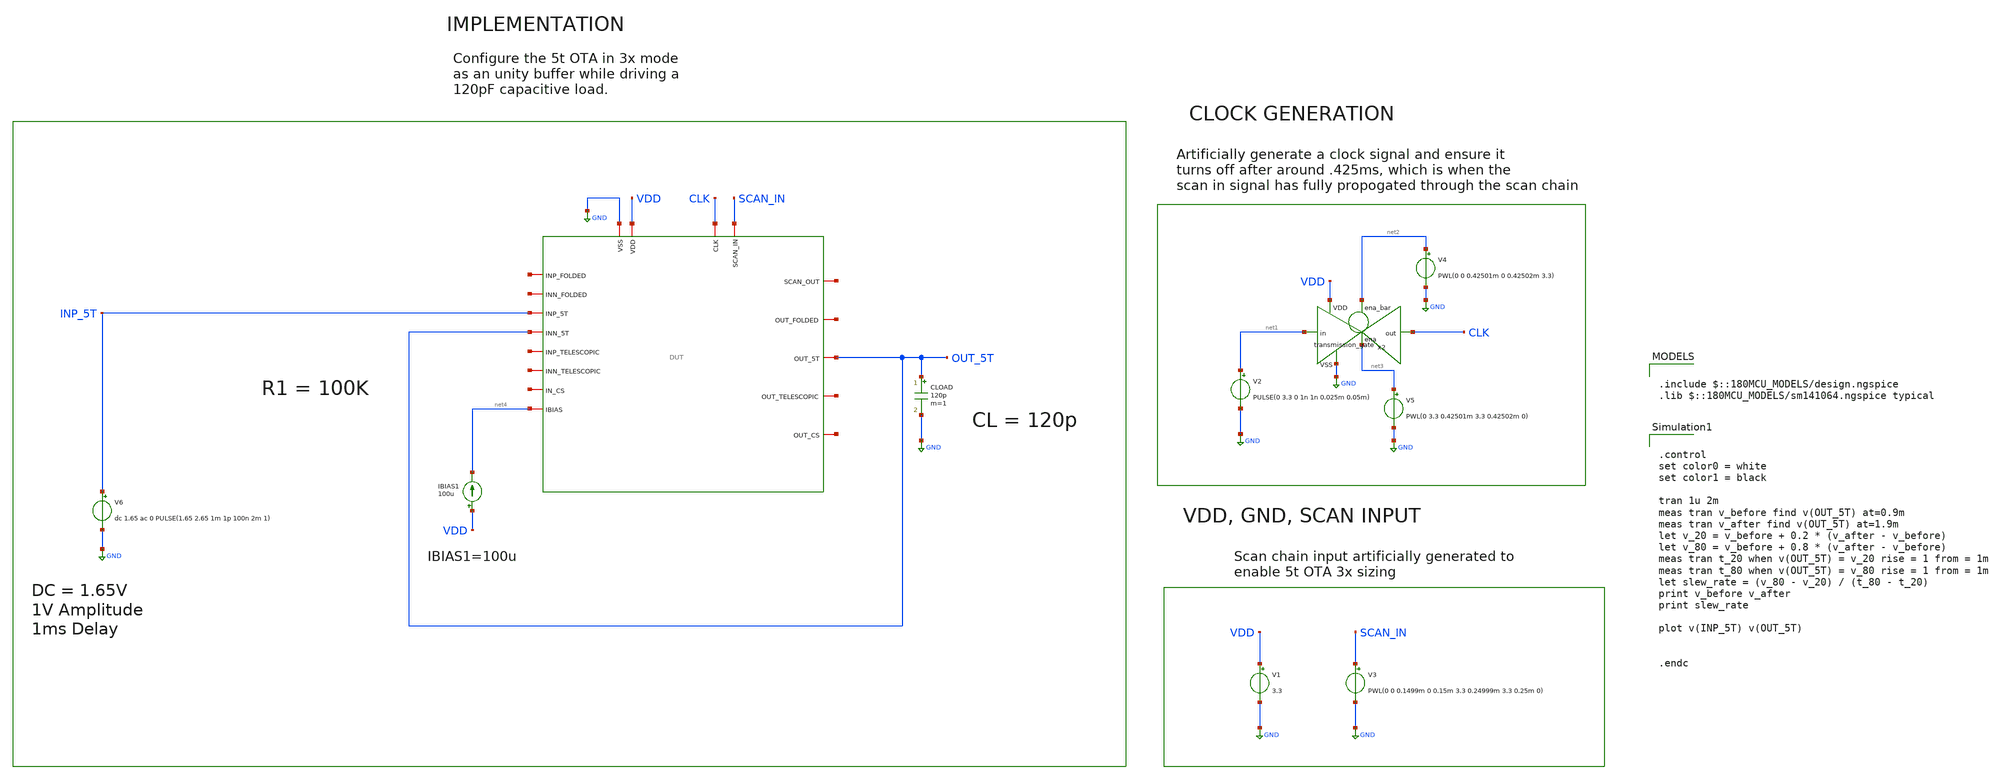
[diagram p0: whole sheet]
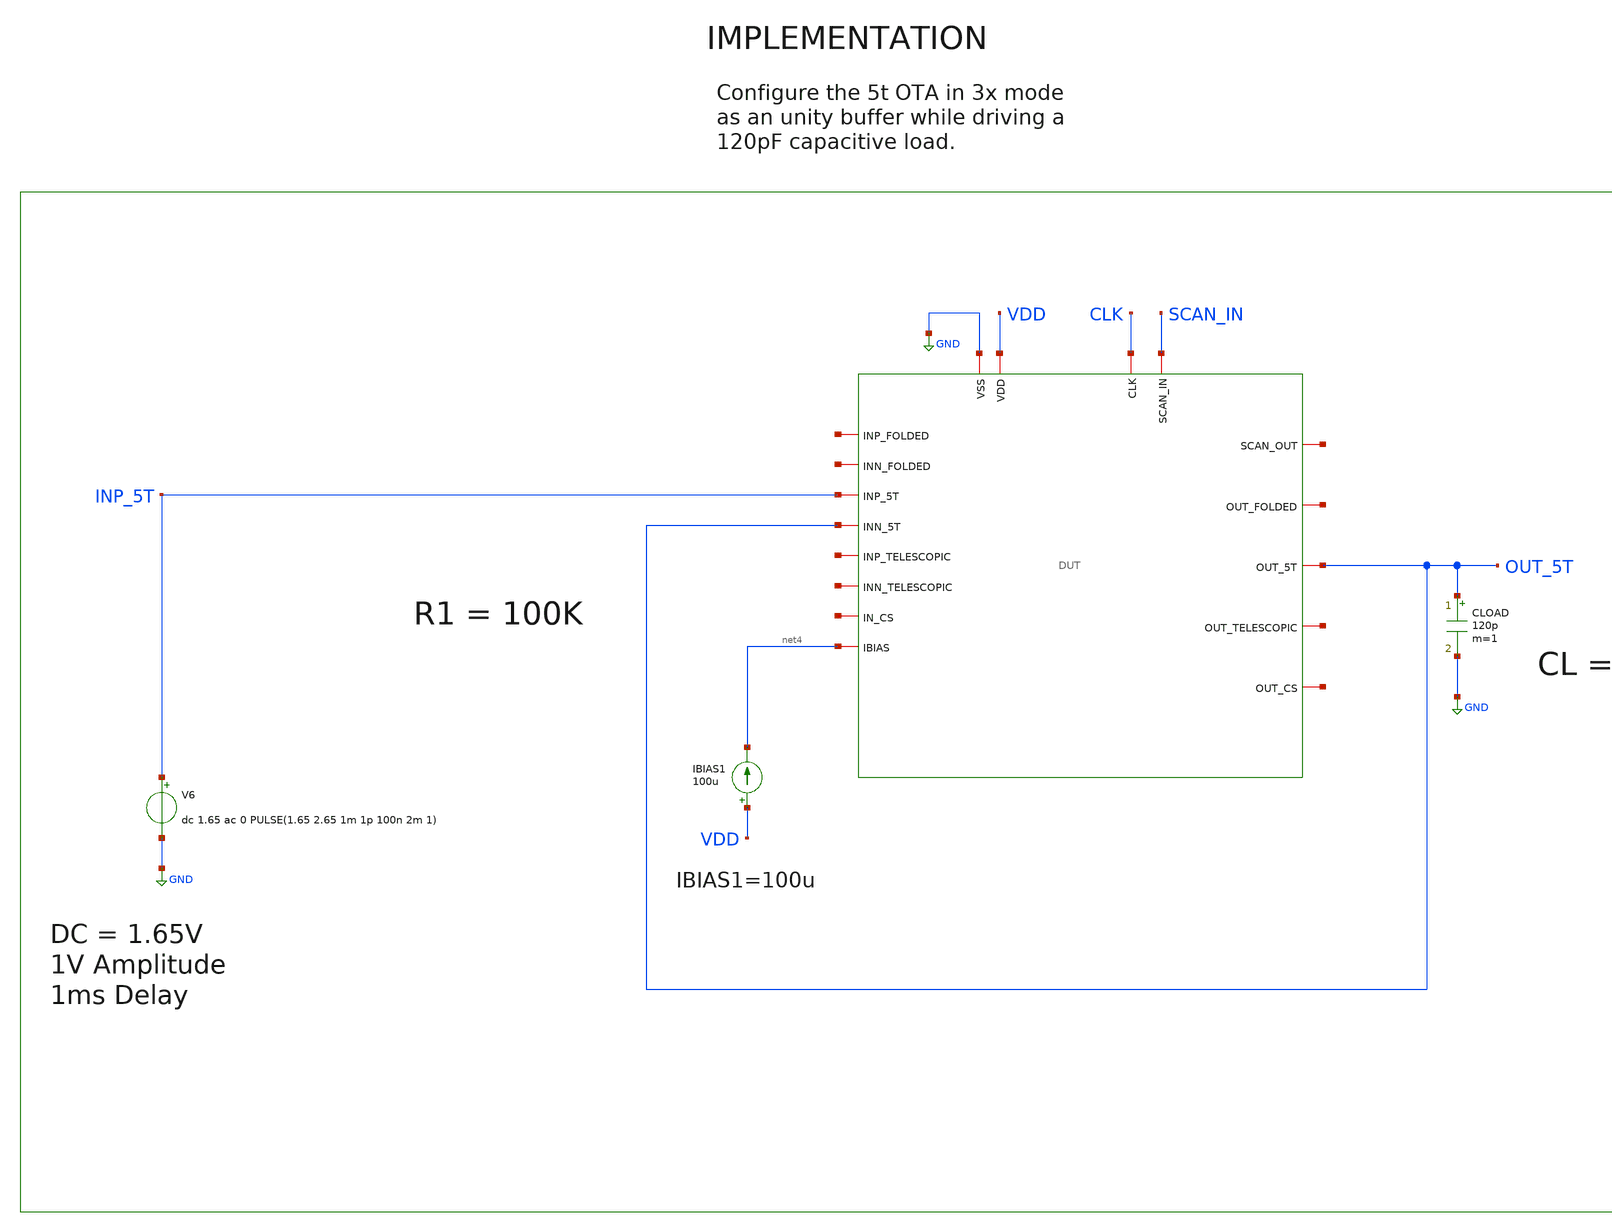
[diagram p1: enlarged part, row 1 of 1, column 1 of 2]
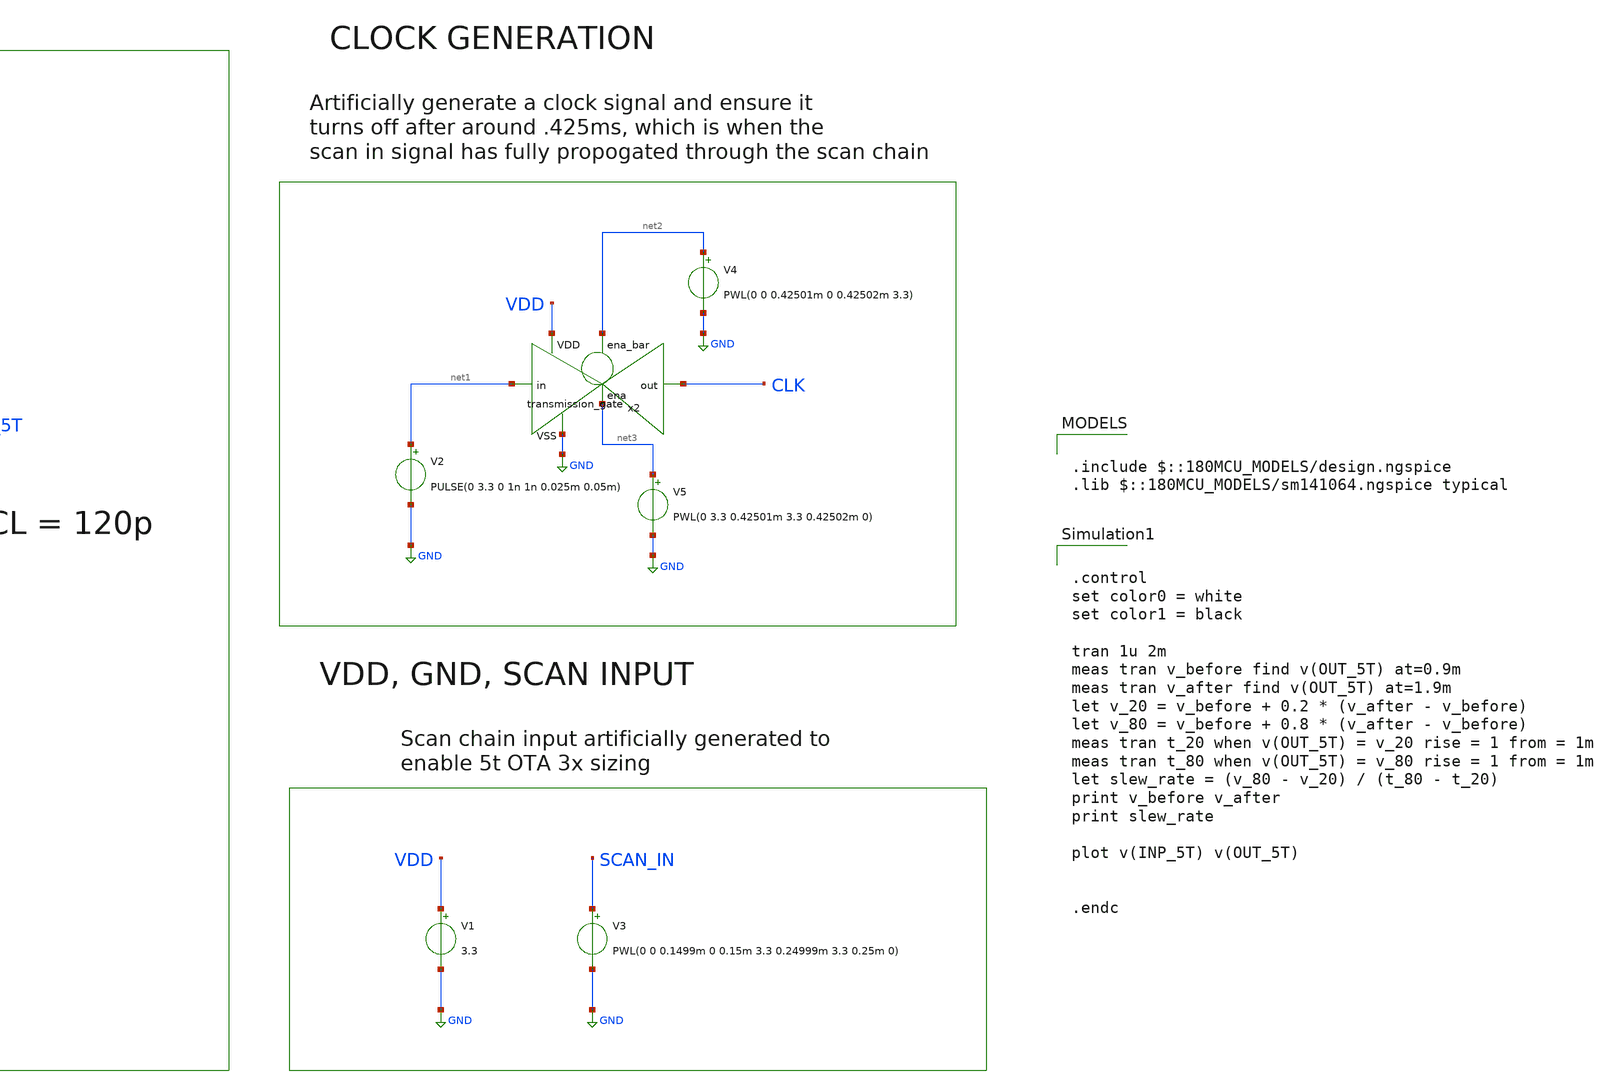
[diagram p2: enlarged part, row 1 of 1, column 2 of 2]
** sch_path: designs/libs/core_tb/sl/ota_5t/5t_tran_SR_3x.sch
**.subckt 5t_tran_SR_3x
V3 SCAN_IN GND PWL(0 0 0.1499m 0 0.15m 3.3 0.24999m 3.3 0.25m 0)
V1 VDD GND 3.3
V2 net1 GND PULSE(0 3.3 0 1n 1n 0.025m 0.05m)
x2 net2 VDD CLK net1 GND net3 transmission_gate
V4 net2 GND PWL(0 0 0.42501m 0 0.42502m 3.3)
V5 net3 GND PWL(0 3.3 0.42501m 3.3 0.42502m 0)
IBIAS1 VDD net4 100u
CLOAD OUT_5T GND 120p m=1
V6 INP_5T GND dc 1.65 ac 0 PULSE(1.65 2.65 1m 1p 100n 2m 1)
x1 CLK net5 SCAN_IN GND VDD net6 net7 OUT_5T net4 net8 INP_5T OUT_5T net9 net10 net11 net12 net13
+ DUT
**** begin user architecture code

.include $::180MCU_MODELS/design.ngspice
.lib $::180MCU_MODELS/sm141064.ngspice typical



.control
set color0 = white
set color1 = black

tran 1u 2m
meas tran v_before find v(OUT_5T) at=0.9m
meas tran v_after find v(OUT_5T) at=1.9m
let v_20 = v_before + 0.2 * (v_after - v_before)
let v_80 = v_before + 0.8 * (v_after - v_before)
meas tran t_20 when v(OUT_5T) = v_20 rise = 1 from = 1m
meas tran t_80 when v(OUT_5T) = v_80 rise = 1 from = 1m
let slew_rate = (v_80 - v_20) / (t_80 - t_20)
print v_before v_after
print slew_rate

plot v(INP_5T) v(OUT_5T)


.endc


**** end user architecture code
**.ends
.GLOBAL GND
.end
